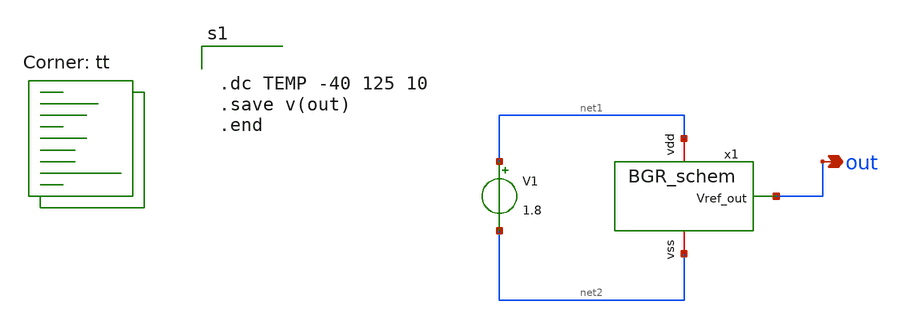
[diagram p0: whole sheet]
** sch_path: TB_BGR.sch
**.subckt TB_BGR out
*.opin out
x1 net1 out net2 BGR_schem
V1 net1 net2 1.8
**** begin user architecture code


.dc TEMP -40 125 10
.save v(out)
.end


.lib $::SKYWATER_MODELS/sky130.lib.spice tt
**** end user architecture code
**.ends

* expanding   symbol:  BGR_schem.sym # of pins=3
** sym_path: BGR_schem.sym
** sch_path: BGR_schem.sch
.subckt BGR_schem vdd Vref_out vss
*.iopin vdd
*.iopin vss
*.opin Vref_out
XM6 net2 net2 net5 vss sky130_fd_pr__nfet_01v8_lvt L=1 W=5 nf=1 ad='int((1 + 1)/2) * 5 / 1 * 0.29' as='int((1 + 2)/2) * 5 / 1 * 0.29'
+ pd='2*int((1 + 1)/2) * (5 / 1 + 0.29)' ps='2*int((1 + 2)/2) * (5 / 1 + 0.29)' nrd='0.29 / 5 ' nrs='0.29 / 5 '
+ sa=0 sb=0 sd=0 mult=8 m=8
XM1 net2 net1 vdd vdd sky130_fd_pr__pfet_01v8_lvt L=2 W=5 nf=1 ad='int((1 + 1)/2) * 5 / 1 * 0.29' as='int((1 + 2)/2) * 5 / 1 * 0.29'
+ pd='2*int((1 + 1)/2) * (5 / 1 + 0.29)' ps='2*int((1 + 2)/2) * (5 / 1 + 0.29)' nrd='0.29 / 5 ' nrs='0.29 / 5 '
+ sa=0 sb=0 sd=0 mult=4 m=4
XQ1 vss vss net4 sky130_fd_pr__pnp_05v5_W3p40L3p40 m=8
XR1 net4 net3 vss sky130_fd_pr__res_high_po W=1 L=14.6 mult=1 m=1
XM3 Vref_out net1 vdd vdd sky130_fd_pr__pfet_01v8_lvt L=2 W=5 nf=1 ad='int((1 + 1)/2) * 5 / 1 * 0.29'
+ as='int((1 + 2)/2) * 5 / 1 * 0.29' pd='2*int((1 + 1)/2) * (5 / 1 + 0.29)' ps='2*int((1 + 2)/2) * (5 / 1 + 0.29)'
+ nrd='0.29 / 5 ' nrs='0.29 / 5 ' sa=0 sb=0 sd=0 mult=4 m=4
XM4 net8 net1 vdd vdd sky130_fd_pr__pfet_01v8_lvt L=1 W=5 nf=1 ad='int((1 + 1)/2) * 5 / 1 * 0.29' as='int((1 + 2)/2) * 5 / 1 * 0.29'
+ pd='2*int((1 + 1)/2) * (5 / 1 + 0.29)' ps='2*int((1 + 2)/2) * (5 / 1 + 0.29)' nrd='0.29 / 5 ' nrs='0.29 / 5 '
+ sa=0 sb=0 sd=0 mult=1 m=1
XM2 net1 net1 vdd vdd sky130_fd_pr__pfet_01v8_lvt L=2 W=5 nf=1 ad='int((1 + 1)/2) * 5 / 1 * 0.29' as='int((1 + 2)/2) * 5 / 1 * 0.29'
+ pd='2*int((1 + 1)/2) * (5 / 1 + 0.29)' ps='2*int((1 + 2)/2) * (5 / 1 + 0.29)' nrd='0.29 / 5 ' nrs='0.29 / 5 '
+ sa=0 sb=0 sd=0 mult=4 m=4
XM5 net6 net1 net8 vdd sky130_fd_pr__pfet_01v8_lvt L=1 W=5 nf=1 ad='int((1 + 1)/2) * 5 / 1 * 0.29' as='int((1 + 2)/2) * 5 / 1 * 0.29'
+ pd='2*int((1 + 1)/2) * (5 / 1 + 0.29)' ps='2*int((1 + 2)/2) * (5 / 1 + 0.29)' nrd='0.29 / 5 ' nrs='0.29 / 5 '
+ sa=0 sb=0 sd=0 mult=1 m=1
XM7 net2 net6 net1 vdd sky130_fd_pr__pfet_01v8_lvt L=1 W=5 nf=1 ad='int((1 + 1)/2) * 5 / 1 * 0.29' as='int((1 + 2)/2) * 5 / 1 * 0.29'
+ pd='2*int((1 + 1)/2) * (5 / 1 + 0.29)' ps='2*int((1 + 2)/2) * (5 / 1 + 0.29)' nrd='0.29 / 5 ' nrs='0.29 / 5 '
+ sa=0 sb=0 sd=0 mult=2 m=2
XM8 net1 net2 net3 vss sky130_fd_pr__nfet_01v8_lvt L=1 W=5 nf=1 ad='int((1 + 1)/2) * 5 / 1 * 0.29' as='int((1 + 2)/2) * 5 / 1 * 0.29'
+ pd='2*int((1 + 1)/2) * (5 / 1 + 0.29)' ps='2*int((1 + 2)/2) * (5 / 1 + 0.29)' nrd='0.29 / 5 ' nrs='0.29 / 5 '
+ sa=0 sb=0 sd=0 mult=8 m=8
XM9 net6 net6 net7 vss sky130_fd_pr__nfet_01v8_lvt L=7 W=1 nf=1 ad='int((1 + 1)/2) * 1 / 1 * 0.29' as='int((1 + 2)/2) * 1 / 1 * 0.29'
+ pd='2*int((1 + 1)/2) * (1 / 1 + 0.29)' ps='2*int((1 + 2)/2) * (1 / 1 + 0.29)' nrd='0.29 / 1 ' nrs='0.29 / 1 '
+ sa=0 sb=0 sd=0 mult=1 m=1
XM10 net7 net7 vss vss sky130_fd_pr__nfet_01v8_lvt L=7 W=1 nf=1 ad='int((1 + 1)/2) * 1 / 1 * 0.29' as='int((1 + 2)/2) * 1 / 1 * 0.29'
+ pd='2*int((1 + 1)/2) * (1 / 1 + 0.29)' ps='2*int((1 + 2)/2) * (1 / 1 + 0.29)' nrd='0.29 / 1 ' nrs='0.29 / 1 '
+ sa=0 sb=0 sd=0 mult=1 m=1
XQ2 vss vss net5 sky130_fd_pr__pnp_05v5_W3p40L3p40 m=1
XQ3 vss vss net9 sky130_fd_pr__pnp_05v5_W3p40L3p40 m=1
XR2 net9 Vref_out vss sky130_fd_pr__res_high_po W=0.1 L=9.21 mult=1 m=1
.ends

.end
